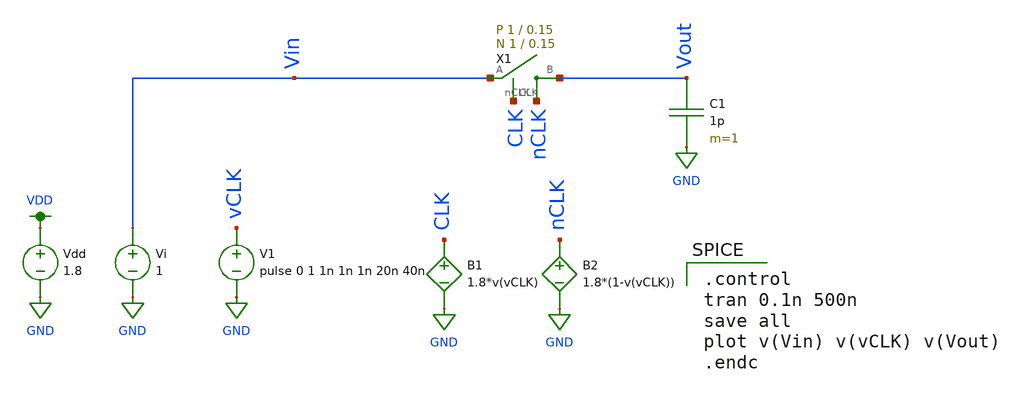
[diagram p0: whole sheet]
** sch_path: schematic/test/switch_test.sch
**.subckt switch_test
C1 Vout GND 1p m=1
V1 vCLK GND pulse 0 1 1n 1n 1n 20n 40n
B1 CLK GND V=1.8*v(vCLK)
B2 nCLK GND V=1.8*(1-v(vCLK))
Vi Vin GND 1
Vdd VDD GND 1.8
X1 Vout Vin CLK nCLK switch Wp=1 Lp=0.15 WW=1 LL=0.15
**** begin user architecture code

.option wnflag=1
.param MC_SWITCH=0.0
.lib ~/skywater/skywater-pdk/libraries/sky130_fd_pr_ngspice/latest/models/sky130.lib.spice tt


.control
tran 0.1n 500n
save all
plot v(Vin) v(vCLK) v(Vout)
.endc

**** end user architecture code
**.ends

* expanding   symbol:  /home/madvlsi/Documents/MADVLSI-Final_Project/schematic/switch.sym # of
*+ pins=4
** sym_path: schematic/switch.sym
** sch_path: schematic/switch.sch
.subckt switch B A CLK nCLK  Wp=1 Lp=0.15 WW=1 LL=0.15
*.iopin B
*.iopin A
*.ipin CLK
*.ipin nCLK
*.ipin CLK
*.ipin CLK
*.ipin nCLK
*.ipin nCLK
XM1 A CLK B GND sky130_fd_pr__nfet_01v8 L={LL} W={WW} nf=1 ad='int((nf+1)/2) * W/nf * 0.29' as='int((nf+2)/2) * W/nf * 0.29'
+ pd='2*int((nf+1)/2) * (W/nf + 0.29)' ps='2*int((nf+2)/2) * (W/nf + 0.29)' nrd='0.29 / W' nrs='0.29 / W'
+ sa=0 sb=0 sd=0 mult=1 m=1
XM2 A nCLK B VDD sky130_fd_pr__pfet_01v8 L={Lp} W={Wp} nf=1 ad='int((nf+1)/2) * W/nf * 0.29' as='int((nf+2)/2) * W/nf * 0.29'
+ pd='2*int((nf+1)/2) * (W/nf + 0.29)' ps='2*int((nf+2)/2) * (W/nf + 0.29)' nrd='0.29 / W' nrs='0.29 / W'
+ sa=0 sb=0 sd=0 mult=1 m=1
XM3 B CLK B VDD sky130_fd_pr__pfet_01v8 L={Lp} W={Wp/2} nf=1 ad='int((nf+1)/2) * W/nf * 0.29' as='int((nf+2)/2) * W/nf * 0.29'
+ pd='2*int((nf+1)/2) * (W/nf + 0.29)' ps='2*int((nf+2)/2) * (W/nf + 0.29)' nrd='0.29 / W' nrs='0.29 / W'
+ sa=0 sb=0 sd=0 mult=1 m=1
XM4 A CLK A VDD sky130_fd_pr__pfet_01v8 L={Lp} W={Wp/2} nf=1 ad='int((nf+1)/2) * W/nf * 0.29' as='int((nf+2)/2) * W/nf * 0.29'
+ pd='2*int((nf+1)/2) * (W/nf + 0.29)' ps='2*int((nf+2)/2) * (W/nf + 0.29)' nrd='0.29 / W' nrs='0.29 / W'
+ sa=0 sb=0 sd=0 mult=1 m=1
XM5 B nCLK B GND sky130_fd_pr__nfet_01v8 L={LL} W={WW/2} nf=1 ad='int((nf+1)/2) * W/nf * 0.29' as='int((nf+2)/2) * W/nf * 0.29'
+ pd='2*int((nf+1)/2) * (W/nf + 0.29)' ps='2*int((nf+2)/2) * (W/nf + 0.29)' nrd='0.29 / W' nrs='0.29 / W'
+ sa=0 sb=0 sd=0 mult=1 m=1
XM6 A nCLK A GND sky130_fd_pr__nfet_01v8 L={LL} W={WW/2} nf=1 ad='int((nf+1)/2) * W/nf * 0.29' as='int((nf+2)/2) * W/nf * 0.29'
+ pd='2*int((nf+1)/2) * (W/nf + 0.29)' ps='2*int((nf+2)/2) * (W/nf + 0.29)' nrd='0.29 / W' nrs='0.29 / W'
+ sa=0 sb=0 sd=0 mult=1 m=1
.ends

.GLOBAL GND
.GLOBAL VDD
.end
